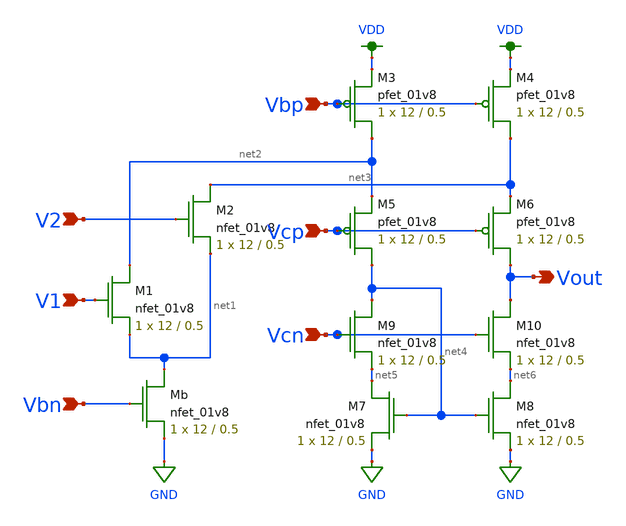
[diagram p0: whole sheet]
** sch_path: MP3/xschem/folded_cascode_diffamp.sch
**.subckt folded_cascode_diffamp V1 V2 Vbn Vbp Vcp Vcn Vout
*.ipin V1
*.ipin V2
*.ipin Vbn
*.ipin Vbp
*.ipin Vcp
*.ipin Vcn
*.opin Vout
XM1 net2 V1 net1 GND sky130_fd_pr__nfet_01v8 L=0.5 W=12 nf=1 ad='int((nf+1)/2) * W/nf * 0.29' as='int((nf+2)/2) * W/nf * 0.29'
+ pd='2*int((nf+1)/2) * (W/nf + 0.29)' ps='2*int((nf+2)/2) * (W/nf + 0.29)' nrd='0.29 / W' nrs='0.29 / W'
+ sa=0 sb=0 sd=0 mult=1 m=1
XM2 net3 V2 net1 GND sky130_fd_pr__nfet_01v8 L=0.5 W=12 nf=1 ad='int((nf+1)/2) * W/nf * 0.29' as='int((nf+2)/2) * W/nf * 0.29'
+ pd='2*int((nf+1)/2) * (W/nf + 0.29)' ps='2*int((nf+2)/2) * (W/nf + 0.29)' nrd='0.29 / W' nrs='0.29 / W'
+ sa=0 sb=0 sd=0 mult=1 m=1
XMb net1 Vbn GND GND sky130_fd_pr__nfet_01v8 L=0.5 W=12 nf=1 ad='int((nf+1)/2) * W/nf * 0.29' as='int((nf+2)/2) * W/nf * 0.29'
+ pd='2*int((nf+1)/2) * (W/nf + 0.29)' ps='2*int((nf+2)/2) * (W/nf + 0.29)' nrd='0.29 / W' nrs='0.29 / W'
+ sa=0 sb=0 sd=0 mult=1 m=1
XM3 net2 Vbp VDD VDD sky130_fd_pr__pfet_01v8 L=0.5 W=12 nf=1 ad='int((nf+1)/2) * W/nf * 0.29' as='int((nf+2)/2) * W/nf * 0.29'
+ pd='2*int((nf+1)/2) * (W/nf + 0.29)' ps='2*int((nf+2)/2) * (W/nf + 0.29)' nrd='0.29 / W' nrs='0.29 / W'
+ sa=0 sb=0 sd=0 mult=1 m=1
XM4 net3 Vbp VDD VDD sky130_fd_pr__pfet_01v8 L=0.5 W=12 nf=1 ad='int((nf+1)/2) * W/nf * 0.29' as='int((nf+2)/2) * W/nf * 0.29'
+ pd='2*int((nf+1)/2) * (W/nf + 0.29)' ps='2*int((nf+2)/2) * (W/nf + 0.29)' nrd='0.29 / W' nrs='0.29 / W'
+ sa=0 sb=0 sd=0 mult=1 m=1
XM5 net4 Vcp net2 VDD sky130_fd_pr__pfet_01v8 L=0.5 W=12 nf=1 ad='int((nf+1)/2) * W/nf * 0.29' as='int((nf+2)/2) * W/nf * 0.29'
+ pd='2*int((nf+1)/2) * (W/nf + 0.29)' ps='2*int((nf+2)/2) * (W/nf + 0.29)' nrd='0.29 / W' nrs='0.29 / W'
+ sa=0 sb=0 sd=0 mult=1 m=1
XM6 Vout Vcp net3 VDD sky130_fd_pr__pfet_01v8 L=0.5 W=12 nf=1 ad='int((nf+1)/2) * W/nf * 0.29' as='int((nf+2)/2) * W/nf * 0.29'
+ pd='2*int((nf+1)/2) * (W/nf + 0.29)' ps='2*int((nf+2)/2) * (W/nf + 0.29)' nrd='0.29 / W' nrs='0.29 / W'
+ sa=0 sb=0 sd=0 mult=1 m=1
XM7 net5 net4 GND GND sky130_fd_pr__nfet_01v8 L=0.5 W=12 nf=1 ad='int((nf+1)/2) * W/nf * 0.29' as='int((nf+2)/2) * W/nf * 0.29'
+ pd='2*int((nf+1)/2) * (W/nf + 0.29)' ps='2*int((nf+2)/2) * (W/nf + 0.29)' nrd='0.29 / W' nrs='0.29 / W'
+ sa=0 sb=0 sd=0 mult=1 m=1
XM8 net6 net4 GND GND sky130_fd_pr__nfet_01v8 L=0.5 W=12 nf=1 ad='int((nf+1)/2) * W/nf * 0.29' as='int((nf+2)/2) * W/nf * 0.29'
+ pd='2*int((nf+1)/2) * (W/nf + 0.29)' ps='2*int((nf+2)/2) * (W/nf + 0.29)' nrd='0.29 / W' nrs='0.29 / W'
+ sa=0 sb=0 sd=0 mult=1 m=1
XM9 net4 Vcn net5 GND sky130_fd_pr__nfet_01v8 L=0.5 W=12 nf=1 ad='int((nf+1)/2) * W/nf * 0.29' as='int((nf+2)/2) * W/nf * 0.29'
+ pd='2*int((nf+1)/2) * (W/nf + 0.29)' ps='2*int((nf+2)/2) * (W/nf + 0.29)' nrd='0.29 / W' nrs='0.29 / W'
+ sa=0 sb=0 sd=0 mult=1 m=1
XM10 Vout Vcn net6 GND sky130_fd_pr__nfet_01v8 L=0.5 W=12 nf=1 ad='int((nf+1)/2) * W/nf * 0.29' as='int((nf+2)/2) * W/nf * 0.29'
+ pd='2*int((nf+1)/2) * (W/nf + 0.29)' ps='2*int((nf+2)/2) * (W/nf + 0.29)' nrd='0.29 / W' nrs='0.29 / W'
+ sa=0 sb=0 sd=0 mult=1 m=1
**.ends
.GLOBAL GND
.GLOBAL VDD
.end
